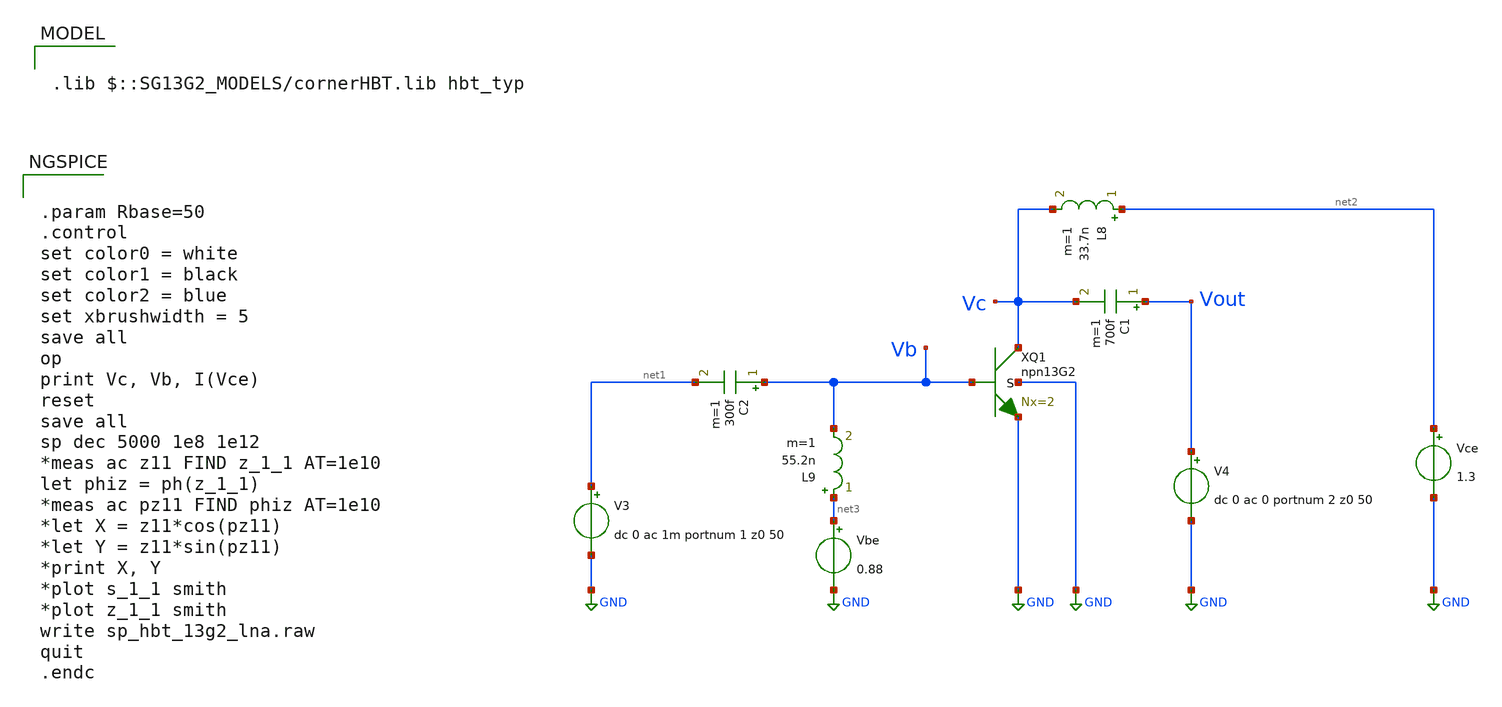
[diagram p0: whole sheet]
** sch_path: ihp-sg13g2/libs.tech/xschem/sg13g2_tests/sp_hbt_13g2.sch
* Copyright 2023 IHP PDK Authors
**.subckt sp_hbt_13g2
V4 Vout GND dc 0 ac 0 portnum 2 z0 50
V3 net1 GND dc 0 ac 1m portnum 1 z0 50
Vce net2 GND 1.3
XQ1 Vc Vb GND GND npn13G2 Nx=2
Vbe net3 GND 0.88
C1 Vout Vc 700f m=1
C2 Vb net1 300f m=1
L8 net2 Vc 33.7n m=1
L9 net3 Vb 55.2n m=1
**** begin user architecture code

.lib $::SG13G2_MODELS/cornerHBT.lib hbt_typ



.param Rbase=50
.control
set color0 = white
set color1 = black
set color2 = blue
set xbrushwidth = 5
save all
op
print Vc, Vb, I(Vce)
reset
save all
sp dec 5000 1e8 1e12
*meas ac z11 FIND z_1_1 AT=1e10
let phiz = ph(z_1_1)
*meas ac pz11 FIND phiz AT=1e10
*let X = z11*cos(pz11)
*let Y = z11*sin(pz11)
*print X, Y
*plot s_1_1 smith
*plot z_1_1 smith
write sp_hbt_13g2_lna.raw
quit
.endc


**** end user architecture code
**.ends
.GLOBAL GND
.end
